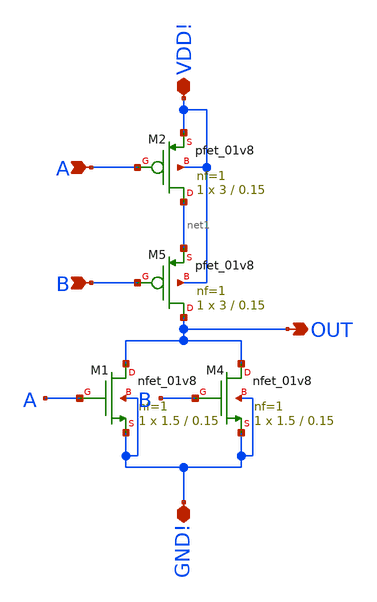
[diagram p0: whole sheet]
** sch_path: skywater_stuff/NOR_VDD_GND.sch
**.subckt NOR_VDD_GND A B OUT VDD! GND!
*.ipin A
*.ipin B
*.opin OUT
*.iopin VDD!
*.iopin GND!
XM1 OUT A GND! GND! sky130_fd_pr__nfet_01v8 L=0.15 W=1.5 nf=1 ad='int((nf+1)/2) * W/nf * 0.29' as='int((nf+2)/2) * W/nf * 0.29'
+ pd='2*int((nf+1)/2) * (W/nf + 0.29)' ps='2*int((nf+2)/2) * (W/nf + 0.29)' nrd='0.29 / W' nrs='0.29 / W'
+ sa=0 sb=0 sd=0 mult=1 m=1
XM4 OUT B GND! GND! sky130_fd_pr__nfet_01v8 L=0.15 W=1.5 nf=1 ad='int((nf+1)/2) * W/nf * 0.29' as='int((nf+2)/2) * W/nf * 0.29'
+ pd='2*int((nf+1)/2) * (W/nf + 0.29)' ps='2*int((nf+2)/2) * (W/nf + 0.29)' nrd='0.29 / W' nrs='0.29 / W'
+ sa=0 sb=0 sd=0 mult=1 m=1
XM5 OUT B net1 VDD! sky130_fd_pr__pfet_01v8 L=0.15 W=3 nf=1 ad='int((nf+1)/2) * W/nf * 0.29' as='int((nf+2)/2) * W/nf * 0.29'
+ pd='2*int((nf+1)/2) * (W/nf + 0.29)' ps='2*int((nf+2)/2) * (W/nf + 0.29)' nrd='0.29 / W' nrs='0.29 / W'
+ sa=0 sb=0 sd=0 mult=1 m=1
XM2 net1 A VDD! VDD! sky130_fd_pr__pfet_01v8 L=0.15 W=3 nf=1 ad='int((nf+1)/2) * W/nf * 0.29' as='int((nf+2)/2) * W/nf * 0.29'
+ pd='2*int((nf+1)/2) * (W/nf + 0.29)' ps='2*int((nf+2)/2) * (W/nf + 0.29)' nrd='0.29 / W' nrs='0.29 / W'
+ sa=0 sb=0 sd=0 mult=1 m=1
**.ends
.end
